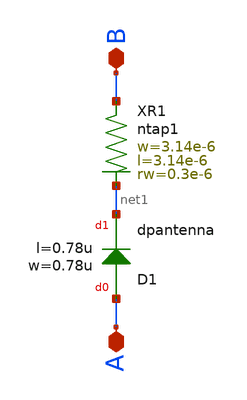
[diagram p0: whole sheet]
** sch_path: ihp-sg13cmos5l/schematic/xschem/sg13_dpantenna.sch
**.subckt sg13_dpantenna A B
*.iopin A
*.iopin B
XD1 A net1 dpantenna l=0.78u w=0.78u
XR1 B net1 ntap1 R=20.06 w=3.14e-6 l=3.14e-6 rw=0.3e-6
**.ends
.end
